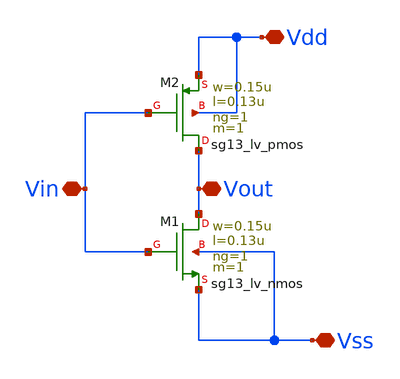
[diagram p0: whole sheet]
** sch_path: design/blocks/inversor/schematic/inversor.sch
**.subckt inversor Vout Vin Vss Vdd
*.iopin Vout
*.iopin Vin
*.iopin Vss
*.iopin Vdd
XM1 Vout Vin Vss Vss sg13_lv_nmos w=0.15u l=0.13u ng=1 m=1 mm_ok=1
XM2 Vout Vin Vdd Vdd sg13_lv_pmos w=0.15u l=0.13u ng=1 m=1 mm_ok=1
**.ends
.end
